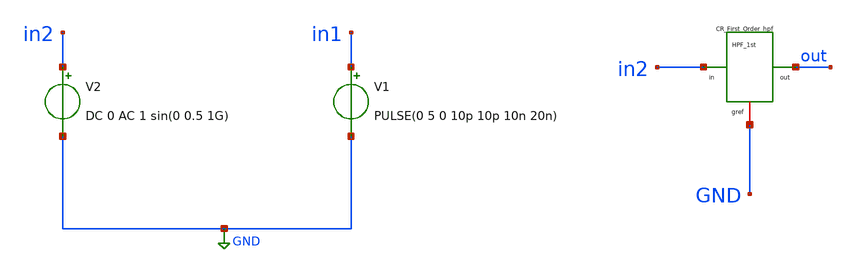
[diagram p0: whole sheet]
** sch_path: testbenches/tb_CR_hpf.sch
**.subckt tb_CR_hpf
x1 in2 out GND CR_First_Order_hpf
V1 in1 GND PULSE(0 5 0 10p 10p 10n 20n)
V2 in2 GND DC 0 AC 1 sin(0 0.5 1G)
**** begin user architecture code



.param temp=27

* =========================
* TRANSIENT ANALYSIS
* =========================

.control

tran 1p 5n
save all
run

* ---------------------------------
* Output Voltage Measurements
* ---------------------------------

set color0 = white

meas tran Vmax MAX v(out)
meas tran Vmin MIN v(out)

* Average Output Voltage
meas tran Vavg AVG v(out)

* ---------------------------------
* Rise Time Measurement
* ---------------------------------
let v90p = 0.9 * Vmax
let v10p = 0.1 * Vmax

meas tran t90p WHEN v(out)=v90p FALL=1
meas tran t10p WHEN v(out)=v10p FALL=1

let RiseTime = t10p - t90p
print RiseTime

* ---------------------------------
* Fall Time Measurement
* ---------------------------------
let V90n = 0.9* Vmin
let v10n = 0.1* Vmin


meas tran t90n WHEN v(out)=v90n RISE=1
meas tran t10n WHEN v(out)=v10n RISE=1

let FallTime = t10n-t90n
print FallTime

* ---------------------------------
* Plot Signals
* ---------------------------------
plot v(in2) v(out)

.endc

* =========================
* AC ANALYSIS (COMMENTED)
* =========================
.ac dec 100 1 100G

.control

save all
run

set color0 = white

** Magnitude in dB
let gain_db = db(v(out))

** Phase Response
let phase_deg = phase(v(out))

** Gain at Cutoff
meas ac Gain_1k FIND gain_db AT=1k

plot gain_db
plot phase_deg

.endc




**** end user architecture code
**.ends

* expanding   symbol:  CR_First_Order_hpf.sym # of pins=3
** sym_path: sch/CR_First_Order_hpf.sym
** sch_path: sch/CR_First_Order_hpf.sch
.subckt CR_First_Order_hpf in out gref
*.ipin in
*.iopin gref
*.opin out
R1 out gref 1k m=1
C1 in out 1p m=1
.ends

.GLOBAL GND
.end
